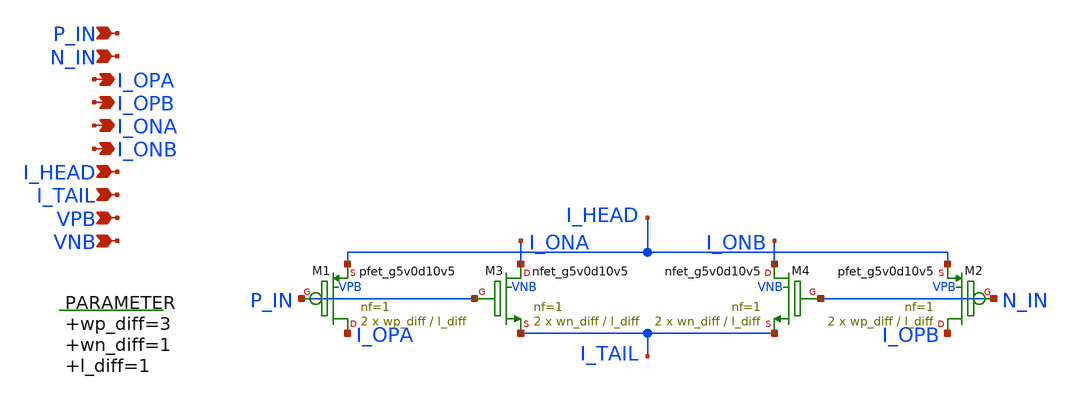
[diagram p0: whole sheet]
** sch_path: xschem/diff_pair.sch
**.subckt diff_pair I_OPA I_OPB P_IN N_IN I_ONA I_ONB I_HEAD I_TAIL VPB VNB
*.opin I_OPA
*.opin I_OPB
*.ipin P_IN
*.ipin N_IN
*.opin I_ONA
*.opin I_ONB
*.ipin I_HEAD
*.ipin I_TAIL
*.ipin VPB
*.ipin VNB
XM1 I_OPA P_IN I_HEAD VPB sky130_fd_pr__pfet_g5v0d10v5 L=l_diff W=wp_diff nf=1 ad='int((nf+1)/2) * W/nf * 0.29'
+ as='int((nf+2)/2) * W/nf * 0.29' pd='2*int((nf+1)/2) * (W/nf + 0.29)' ps='2*int((nf+2)/2) * (W/nf + 0.29)'
+ nrd='0.29 / W' nrs='0.29 / W' sa=0 sb=0 sd=0 mult=2 m=2
XM3 I_ONA P_IN I_TAIL VNB sky130_fd_pr__nfet_g5v0d10v5 L=l_diff W=wn_diff nf=1 ad='int((nf+1)/2) * W/nf * 0.29'
+ as='int((nf+2)/2) * W/nf * 0.29' pd='2*int((nf+1)/2) * (W/nf + 0.29)' ps='2*int((nf+2)/2) * (W/nf + 0.29)'
+ nrd='0.29 / W' nrs='0.29 / W' sa=0 sb=0 sd=0 mult=2 m=2
.param wp_diff=3 wn_diff=1 l_diff=1

XM2 I_OPB N_IN I_HEAD VPB sky130_fd_pr__pfet_g5v0d10v5 L=l_diff W=wp_diff nf=1 ad='int((nf+1)/2) * W/nf * 0.29'
+ as='int((nf+2)/2) * W/nf * 0.29' pd='2*int((nf+1)/2) * (W/nf + 0.29)' ps='2*int((nf+2)/2) * (W/nf + 0.29)'
+ nrd='0.29 / W' nrs='0.29 / W' sa=0 sb=0 sd=0 mult=2 m=2
XM4 I_ONB N_IN I_TAIL VNB sky130_fd_pr__nfet_g5v0d10v5 L=l_diff W=wn_diff nf=1 ad='int((nf+1)/2) * W/nf * 0.29'
+ as='int((nf+2)/2) * W/nf * 0.29' pd='2*int((nf+1)/2) * (W/nf + 0.29)' ps='2*int((nf+2)/2) * (W/nf + 0.29)'
+ nrd='0.29 / W' nrs='0.29 / W' sa=0 sb=0 sd=0 mult=2 m=2
**.ends
.end
